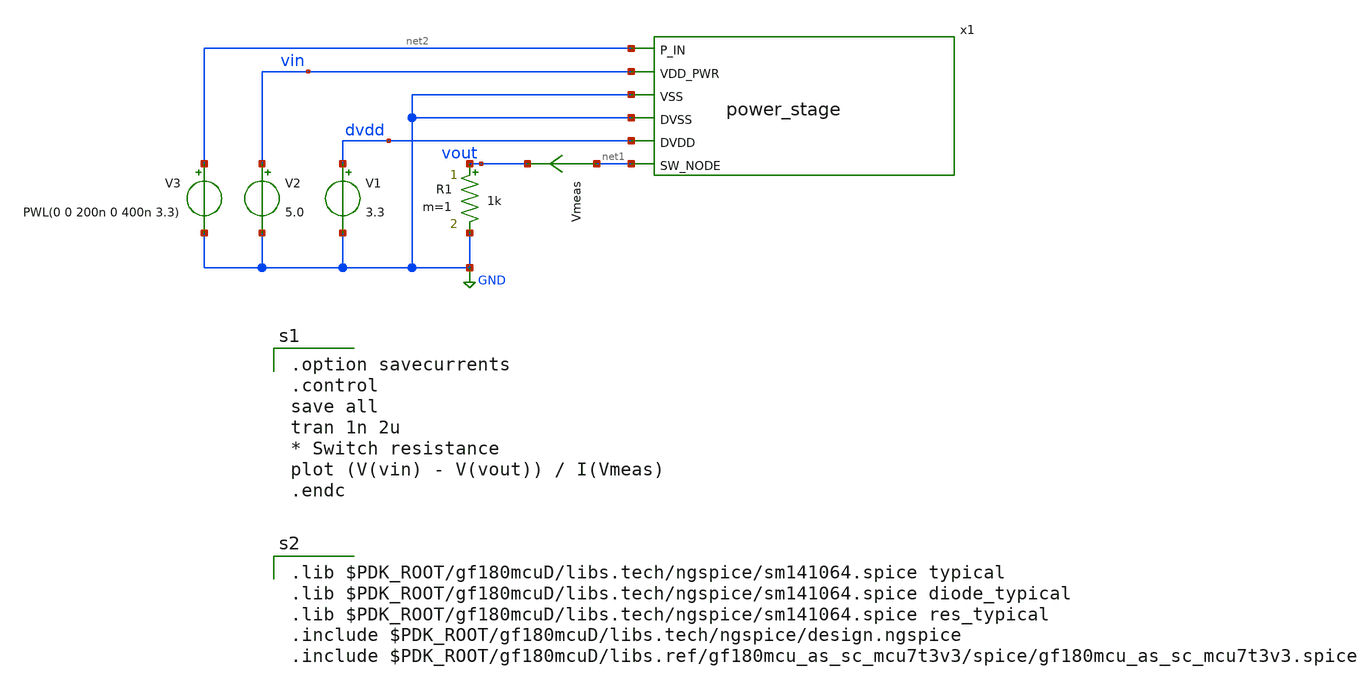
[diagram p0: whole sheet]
** sch_path: xschem/power_stage_tb.sch
**.subckt power_stage_tb
x1 net2 vin GND GND dvdd net1 power_stage
Vmeas net1 vout 0
.save i(vmeas)
R1 vout GND 1k m=1
V1 dvdd GND 3.3
V2 vin GND 5.0
V3 net2 GND PWL(0 0 200n 0 400n 3.3)
**** begin user architecture code

.option savecurrents
.control
save all
tran 1n 2u
* Switch resistance
plot (V(vin) - V(vout)) / I(Vmeas)
.endc


.lib $PDK_ROOT/gf180mcuD/libs.tech/ngspice/sm141064.spice typical
.lib $PDK_ROOT/gf180mcuD/libs.tech/ngspice/sm141064.spice diode_typical
.lib $PDK_ROOT/gf180mcuD/libs.tech/ngspice/sm141064.spice res_typical
.include $PDK_ROOT/gf180mcuD/libs.tech/ngspice/design.ngspice
.include $PDK_ROOT/gf180mcuD/libs.ref/gf180mcu_as_sc_mcu7t3v3/spice/gf180mcu_as_sc_mcu7t3v3.spice

**** end user architecture code
**.ends
.GLOBAL GND
.end
